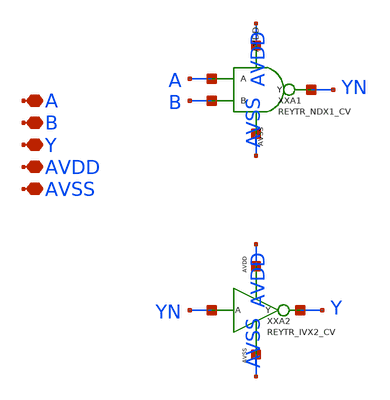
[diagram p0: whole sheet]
** sch_path: design/REY_TR_SKY130A/REYTR_ANX2_CV.sch
**.subckt REYTR_ANX2_CV A B Y AVDD AVSS
*.iopin A
*.iopin B
*.iopin Y
*.iopin AVDD
*.iopin AVSS
XXA1 A B YN AVDD AVSS REYTR_NDX1_CV
XXA2 YN Y AVDD AVSS REYTR_IVX2_CV xoffset=0 yoffset=0 angle=0 M=1
**.ends
.end
